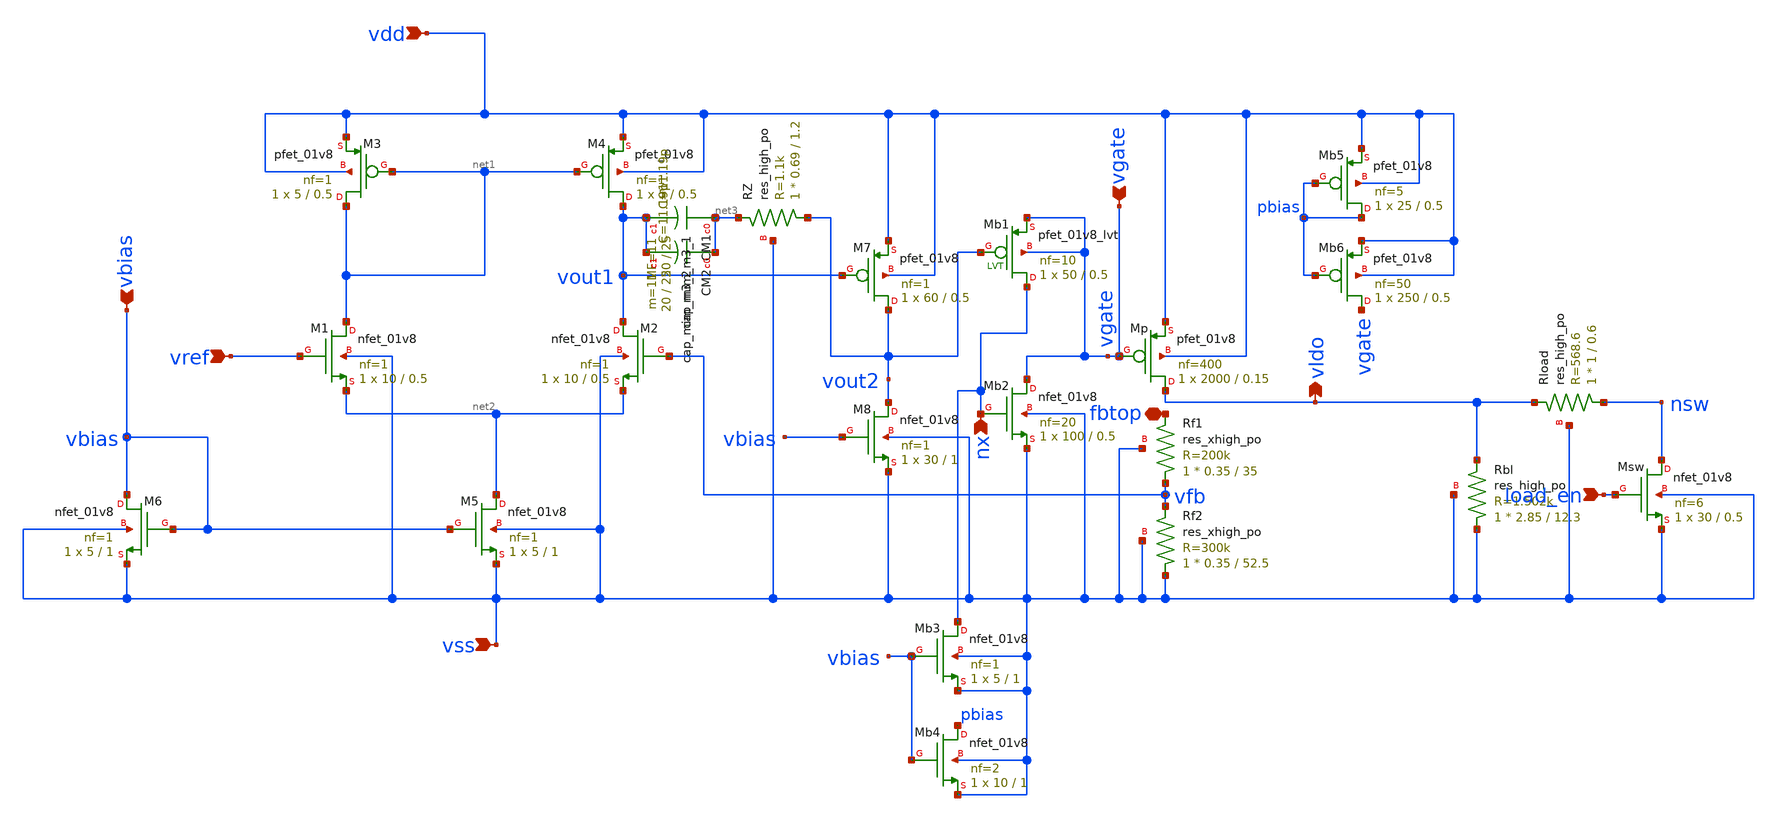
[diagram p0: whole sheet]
** sch_path: src/schematics/ldo_chip.sch
**.subckt ldo_chip vdd vss vref vldo load_en fbtop vbias nx vgate
*.ipin vdd
*.ipin vss
*.ipin vref
*.opin vldo
*.ipin load_en
*.iopin fbtop
*.ipin vbias
*.ipin nx
*.ipin vgate
XM1 net1 vref net2 vss sky130_fd_pr__nfet_01v8 L=0.5 W=10 nf=1 ad='int((1 + 1)/2) * 10 / 1 * 0.29' as='int((1 + 2)/2) * 10 / 1 * 0.29'
+ pd='2*int((1 + 1)/2) * (10 / 1 + 0.29)' ps='2*int((1 + 2)/2) * (10 / 1 + 0.29)' nrd='0.29 / 10 ' nrs='0.29 / 10 '
+ sa=0 sb=0 sd=0 mult=1 m=1
XM2 vout1 vfb net2 vss sky130_fd_pr__nfet_01v8 L=0.5 W=10 nf=1 ad='int((1 + 1)/2) * 10 / 1 * 0.29' as='int((1 + 2)/2) * 10 / 1 * 0.29'
+ pd='2*int((1 + 1)/2) * (10 / 1 + 0.29)' ps='2*int((1 + 2)/2) * (10 / 1 + 0.29)' nrd='0.29 / 10 ' nrs='0.29 / 10 '
+ sa=0 sb=0 sd=0 mult=1 m=1
XM3 net1 net1 vdd vdd sky130_fd_pr__pfet_01v8 L=0.5 W=5 nf=1 ad='int((1 + 1)/2) * 5 / 1 * 0.29' as='int((1 + 2)/2) * 5 / 1 * 0.29'
+ pd='2*int((1 + 1)/2) * (5 / 1 + 0.29)' ps='2*int((1 + 2)/2) * (5 / 1 + 0.29)' nrd='0.29 / 5 ' nrs='0.29 / 5 '
+ sa=0 sb=0 sd=0 mult=1 m=1
XM4 vout1 net1 vdd vdd sky130_fd_pr__pfet_01v8 L=0.5 W=5 nf=1 ad='int((1 + 1)/2) * 5 / 1 * 0.29' as='int((1 + 2)/2) * 5 / 1 * 0.29'
+ pd='2*int((1 + 1)/2) * (5 / 1 + 0.29)' ps='2*int((1 + 2)/2) * (5 / 1 + 0.29)' nrd='0.29 / 5 ' nrs='0.29 / 5 '
+ sa=0 sb=0 sd=0 mult=1 m=1
XM5 net2 vbias vss vss sky130_fd_pr__nfet_01v8 L=1 W=5 nf=1 ad='int((1 + 1)/2) * 5 / 1 * 0.29' as='int((1 + 2)/2) * 5 / 1 * 0.29'
+ pd='2*int((1 + 1)/2) * (5 / 1 + 0.29)' ps='2*int((1 + 2)/2) * (5 / 1 + 0.29)' nrd='0.29 / 5 ' nrs='0.29 / 5 '
+ sa=0 sb=0 sd=0 mult=1 m=1
XM6 vbias vbias vss vss sky130_fd_pr__nfet_01v8 L=1 W=5 nf=1 ad='int((1 + 1)/2) * 5 / 1 * 0.29' as='int((1 + 2)/2) * 5 / 1 * 0.29'
+ pd='2*int((1 + 1)/2) * (5 / 1 + 0.29)' ps='2*int((1 + 2)/2) * (5 / 1 + 0.29)' nrd='0.29 / 5 ' nrs='0.29 / 5 '
+ sa=0 sb=0 sd=0 mult=1 m=1
XM7 vout2 vout1 vdd vdd sky130_fd_pr__pfet_01v8 L=0.5 W=60 nf=1 ad='int((1 + 1)/2) * 60 / 1 * 0.29' as='int((1 + 2)/2) * 60 / 1 * 0.29'
+ pd='2*int((1 + 1)/2) * (60 / 1 + 0.29)' ps='2*int((1 + 2)/2) * (60 / 1 + 0.29)' nrd='0.29 / 60 ' nrs='0.29 / 60 '
+ sa=0 sb=0 sd=0 mult=1 m=1
XM8 vout2 vbias vss vss sky130_fd_pr__nfet_01v8 L=1 W=30 nf=1 ad='int((1 + 1)/2) * 30 / 1 * 0.29' as='int((1 + 2)/2) * 30 / 1 * 0.29'
+ pd='2*int((1 + 1)/2) * (30 / 1 + 0.29)' ps='2*int((1 + 2)/2) * (30 / 1 + 0.29)' nrd='0.29 / 30 ' nrs='0.29 / 30 '
+ sa=0 sb=0 sd=0 mult=1 m=1
XMp vldo vgate vdd vdd sky130_fd_pr__pfet_01v8 L=0.15 W=2000 nf=400 ad='int((400 + 1)/2) * 2000 / 400 * 0.29'
+ as='int((400 + 2)/2) * 2000 / 400 * 0.29' pd='2*int((400 + 1)/2) * (2000 / 400 + 0.29)' ps='2*int((400 + 2)/2) * (2000 / 400 + 0.29)'
+ nrd='0.29 / 2000 ' nrs='0.29 / 2000 ' sa=0 sb=0 sd=0 mult=1 m=1
XMb2 vgate nx vss vss sky130_fd_pr__nfet_01v8 L=0.5 W=100 nf=20 ad='int((20 + 1)/2) * 100 / 20 * 0.29'
+ as='int((20 + 2)/2) * 100 / 20 * 0.29' pd='2*int((20 + 1)/2) * (100 / 20 + 0.29)' ps='2*int((20 + 2)/2) * (100 / 20 + 0.29)'
+ nrd='0.29 / 100 ' nrs='0.29 / 100 ' sa=0 sb=0 sd=0 mult=1 m=1
XMb1 nx vout2 vgate vgate sky130_fd_pr__pfet_01v8_lvt L=0.5 W=50 nf=10 ad='int((10 + 1)/2) * 50 / 10 * 0.29'
+ as='int((10 + 2)/2) * 50 / 10 * 0.29' pd='2*int((10 + 1)/2) * (50 / 10 + 0.29)' ps='2*int((10 + 2)/2) * (50 / 10 + 0.29)'
+ nrd='0.29 / 50 ' nrs='0.29 / 50 ' sa=0 sb=0 sd=0 mult=1 m=1
XMsw nsw load_en vss vss sky130_fd_pr__nfet_01v8 L=0.5 W=30 nf=6 ad='int((6 + 1)/2) * 30 / 6 * 0.29'
+ as='int((6 + 2)/2) * 30 / 6 * 0.29' pd='2*int((6 + 1)/2) * (30 / 6 + 0.29)' ps='2*int((6 + 2)/2) * (30 / 6 + 0.29)'
+ nrd='0.29 / 30 ' nrs='0.29 / 30 ' sa=0 sb=0 sd=0 mult=1 m=1
XRload nsw vldo vss sky130_fd_pr__res_high_po W=1 L=0.6 mult=1 m=1
XCM1 net3 vout1 sky130_fd_pr__cap_mim_m3_1 W=20 L=25 MF=11 m=11
XCM2 net3 vout1 sky130_fd_pr__cap_mim_m3_2 W=20 L=25 MF=11 m=11
XRZ vout2 net3 vss sky130_fd_pr__res_high_po W=0.69 L=1.2 mult=1 m=1
XRbl vss vldo vss sky130_fd_pr__res_high_po W=2.85 L=12.3 mult=1 m=1
XRf1 vfb fbtop vss sky130_fd_pr__res_xhigh_po W=0.35 L=35 mult=1 m=1
XRf2 vss vfb vss sky130_fd_pr__res_xhigh_po W=0.35 L=52.5 mult=1 m=1
XMb3 nx vbias vss vss sky130_fd_pr__nfet_01v8 L=1 W=5 nf=1 ad='int((1 + 1)/2) * 5 / 1 * 0.29' as='int((1 + 2)/2) * 5 / 1 * 0.29'
+ pd='2*int((1 + 1)/2) * (5 / 1 + 0.29)' ps='2*int((1 + 2)/2) * (5 / 1 + 0.29)' nrd='0.29 / 5 ' nrs='0.29 / 5 '
+ sa=0 sb=0 sd=0 mult=1 m=1
XMb4 pbias vbias vss vss sky130_fd_pr__nfet_01v8 L=1 W=10 nf=2 ad='int((2 + 1)/2) * 10 / 2 * 0.29' as='int((2 + 2)/2) * 10 / 2 * 0.29'
+ pd='2*int((2 + 1)/2) * (10 / 2 + 0.29)' ps='2*int((2 + 2)/2) * (10 / 2 + 0.29)' nrd='0.29 / 10 ' nrs='0.29 / 10 '
+ sa=0 sb=0 sd=0 mult=1 m=1
XMb5 pbias pbias vdd vdd sky130_fd_pr__pfet_01v8 L=0.5 W=25 nf=5 ad='int((5 + 1)/2) * 25 / 5 * 0.29'
+ as='int((5 + 2)/2) * 25 / 5 * 0.29' pd='2*int((5 + 1)/2) * (25 / 5 + 0.29)' ps='2*int((5 + 2)/2) * (25 / 5 + 0.29)'
+ nrd='0.29 / 25 ' nrs='0.29 / 25 ' sa=0 sb=0 sd=0 mult=1 m=1
XMb6 vgate pbias vdd vdd sky130_fd_pr__pfet_01v8 L=0.5 W=250 nf=50 ad='int((50 + 1)/2) * 250 / 50 * 0.29'
+ as='int((50 + 2)/2) * 250 / 50 * 0.29' pd='2*int((50 + 1)/2) * (250 / 50 + 0.29)' ps='2*int((50 + 2)/2) * (250 / 50 + 0.29)'
+ nrd='0.29 / 250 ' nrs='0.29 / 250 ' sa=0 sb=0 sd=0 mult=1 m=1
**.ends
.end
